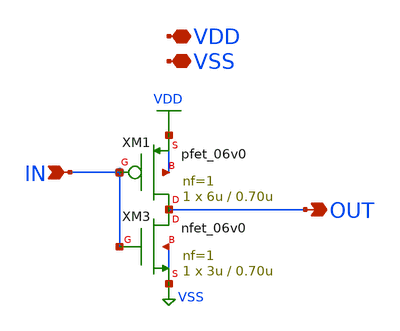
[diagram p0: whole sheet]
** sch_path: xschem/io_inv_2.sch
* Copyright 2023 David Mitchell Bailey
* Licensed under the Apache License, Version 2.0 (the "License");
* you may not use this file except in compliance with the License.
* You may obtain a copy of the License at
* https://www.apache.org/licenses/LICENSE-2.0
* Unless required by applicable law or agreed to in writing, software
* distributed under the License is distributed on an "AS IS" BASIS,
* WITHOUT WARRANTIES OR CONDITIONS OF ANY KIND, either express or implied.
* See the License for the specific language governing permissions and
* limitations under the License.
**.subckt io_inv_2 OUT IN VDD VSS
*.opin OUT
*.ipin IN
*.iopin VDD
*.iopin VSS
XM1 OUT IN VDD VDD pfet_06v0 L=0.70u W=6u nf=1 ad='int((nf+1)/2) * W/nf * 0.18u' as='int((nf+2)/2) * W/nf * 0.18u'
+ pd='2*int((nf+1)/2) * (W/nf + 0.18u)' ps='2*int((nf+2)/2) * (W/nf + 0.18u)' nrd='0.18u / W' nrs='0.18u / W'
+ sa=0 sb=0 sd=0 m=1
XM3 OUT IN VSS VSS nfet_06v0 L=0.70u W=3u nf=1 ad='int((nf+1)/2) * W/nf * 0.18u' as='int((nf+2)/2) * W/nf * 0.18u'
+ pd='2*int((nf+1)/2) * (W/nf + 0.18u)' ps='2*int((nf+2)/2) * (W/nf + 0.18u)' nrd='0.18u / W' nrs='0.18u / W'
+ sa=0 sb=0 sd=0 m=1
**.ends
.GLOBAL VSS
.GLOBAL VDD
.end
